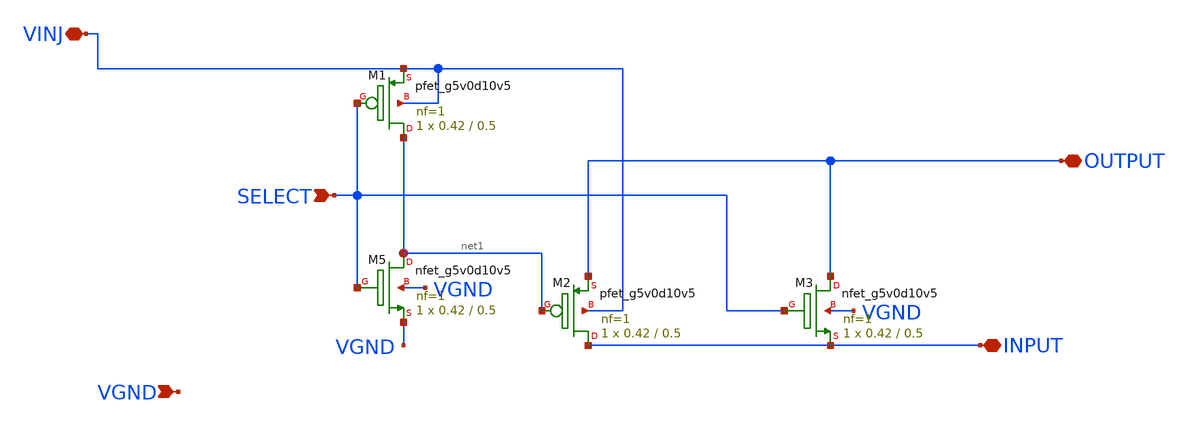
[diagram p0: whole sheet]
** sch_path: sky130_cells/RDAC/Design/Tgate.sch
**.subckt Tgate VINJ SELECT INPUT OUTPUT VGND
*.iopin VINJ
*.ipin SELECT
*.iopin INPUT
*.iopin OUTPUT
*.ipin VGND
XM5 net1 SELECT VGND VGND sky130_fd_pr__nfet_g5v0d10v5 L=0.5 W=0.42 nf=1 ad='int((1 + 1)/2) * 0.42 / 1 * 0.29'
+ as='int((1 + 2)/2) * 0.42 / 1 * 0.29' pd='2*int((1 + 1)/2) * (0.42 / 1 + 0.29)' ps='2*int((1 + 2)/2) * (0.42 / 1 + 0.29)'
+ nrd='0.29 / 0.42 ' nrs='0.29 / 0.42 ' sa=0 sb=0 sd=0 mult=1 m=1
XM1 net1 SELECT VINJ VINJ sky130_fd_pr__pfet_g5v0d10v5 L=0.5 W=0.42 nf=1 ad='int((1 + 1)/2) * 0.42 / 1 * 0.29'
+ as='int((1 + 2)/2) * 0.42 / 1 * 0.29' pd='2*int((1 + 1)/2) * (0.42 / 1 + 0.29)' ps='2*int((1 + 2)/2) * (0.42 / 1 + 0.29)'
+ nrd='0.29 / 0.42 ' nrs='0.29 / 0.42 ' sa=0 sb=0 sd=0 mult=1 m=1
XM2 INPUT net1 OUTPUT VINJ sky130_fd_pr__pfet_g5v0d10v5 L=0.5 W=0.42 nf=1 ad='int((1 + 1)/2) * 0.42 / 1 * 0.29'
+ as='int((1 + 2)/2) * 0.42 / 1 * 0.29' pd='2*int((1 + 1)/2) * (0.42 / 1 + 0.29)' ps='2*int((1 + 2)/2) * (0.42 / 1 + 0.29)'
+ nrd='0.29 / 0.42 ' nrs='0.29 / 0.42 ' sa=0 sb=0 sd=0 mult=1 m=1
XM3 OUTPUT SELECT INPUT VGND sky130_fd_pr__nfet_g5v0d10v5 L=0.5 W=0.42 nf=1 ad='int((1 + 1)/2) * 0.42 / 1 * 0.29'
+ as='int((1 + 2)/2) * 0.42 / 1 * 0.29' pd='2*int((1 + 1)/2) * (0.42 / 1 + 0.29)' ps='2*int((1 + 2)/2) * (0.42 / 1 + 0.29)'
+ nrd='0.29 / 0.42 ' nrs='0.29 / 0.42 ' sa=0 sb=0 sd=0 mult=1 m=1
**.ends
.end
